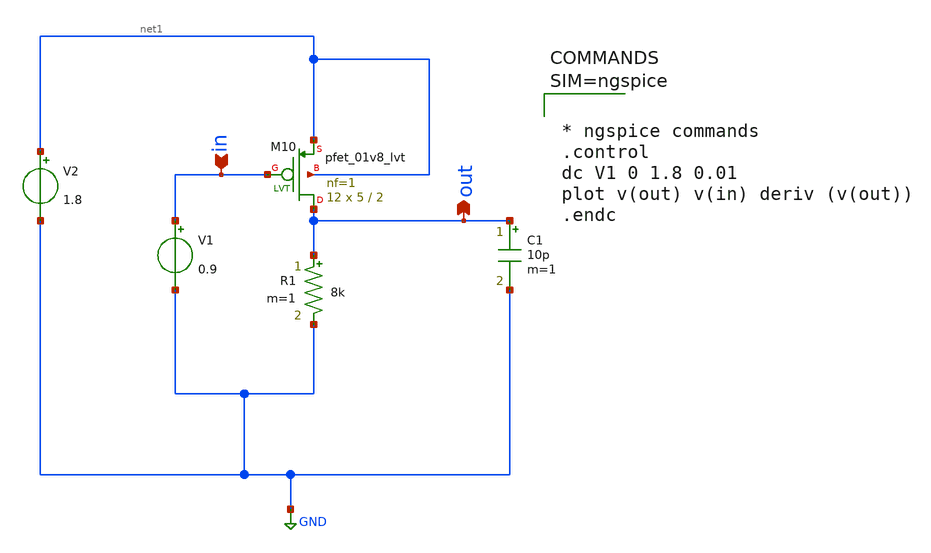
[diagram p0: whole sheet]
** sch_path: xschem/pmos_dc.sch
**.subckt pmos_dc in out
*.ipin in
*.opin out
XM10 out in net1 net1 sky130_fd_pr__pfet_01v8_lvt L=2 W=5 nf=1 ad='int((1 + 1)/2) * 5 / 1 * 0.29' as='int((1 + 2)/2) * 5 / 1 * 0.29'
+ pd='2*int((1 + 1)/2) * (5 / 1 + 0.29)' ps='2*int((1 + 2)/2) * (5 / 1 + 0.29)' nrd='0.29 / 5 ' nrs='0.29 / 5 '
+ sa=0 sb=0 sd=0 mult=12 m=12
R1 out GND 8k m=1
V1 in GND 0.9
C1 out GND 10p m=1
V2 net1 GND 1.8
**** begin user architecture code

** opencircuitdesign pdks install
.lib $::SKYWATER_MODELS/sky130.lib.spice tt




* ngspice commands
.control
dc V1 0 1.8 0.01
plot v(out) v(in) deriv (v(out))
.endc



**** end user architecture code
**.ends
.GLOBAL GND
.end
